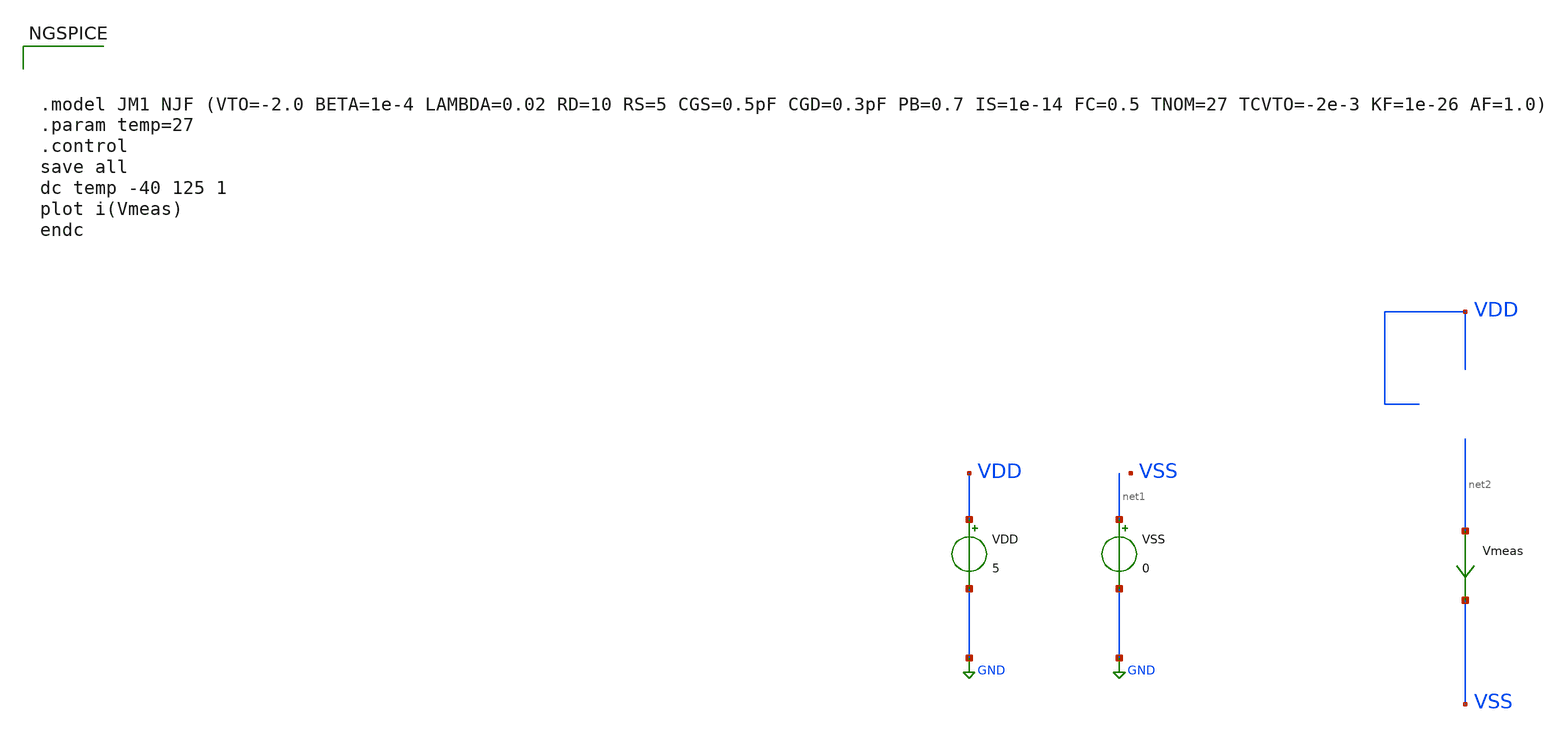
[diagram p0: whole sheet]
** sch_path: Learning/single_ended_amplifiers/A_High_Precision_Micropower_Operational_Amplifier_custom_models/current_reference/testbench.sch

.model JM1 NJF (VTO=-2.0 BETA=1.0E-4 LAMBDA=0.02 RD=10 RS=5 CGS=5pF CGD=3pF PB=0.7 IS=1E-14 FC=0.5)


**.subckt testbench
VDD VDD GND 5
VSS net1 GND 0
Vmeas net2 VSS 0
.save i(vmeas)
**** begin user architecture code



.model JM1 NJF (VTO=-2.0 BETA=1e-4 LAMBDA=0.02 RD=10 RS=5 CGS=0.5pF CGD=0.3pF PB=0.7 IS=1e-14 FC=0.5
+ TNOM=27 TCVTO=-2e-3 KF=1e-26 AF=1.0)
.param temp=27
.control
save all
dc temp -40 125 1
plot i(Vmeas)
endc


**** end user architecture code
**.ends
.GLOBAL GND
.end
